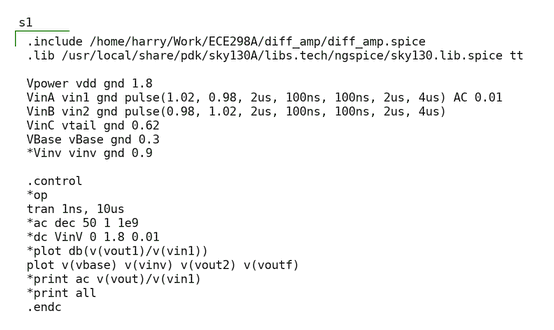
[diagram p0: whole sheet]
** sch_path: magic_xschem_ngspice/Magic_sim.sch
**.subckt Magic_sim
**** begin user architecture code

.include /home/harry/Work/ECE298A/diff_amp/diff_amp.spice
.lib /usr/local/share/pdk/sky130A/libs.tech/ngspice/sky130.lib.spice tt

Vpower vdd gnd 1.8
VinA vin1 gnd pulse(1.02, 0.98, 2us, 100ns, 100ns, 2us, 4us) AC 0.01
VinB vin2 gnd pulse(0.98, 1.02, 2us, 100ns, 100ns, 2us, 4us)
VinC vtail gnd 0.62
VBase vBase gnd 0.3
*Vinv vinv gnd 0.9

.control
*op
tran 1ns, 10us
*ac dec 50 1 1e9
*dc VinV 0 1.8 0.01
*plot db(v(vout1)/v(vin1))
plot v(vbase) v(vinv) v(vout2) v(voutf)
*print ac v(vout)/v(vin1)
*print all
.endc

**** end user architecture code
**.ends
.end
